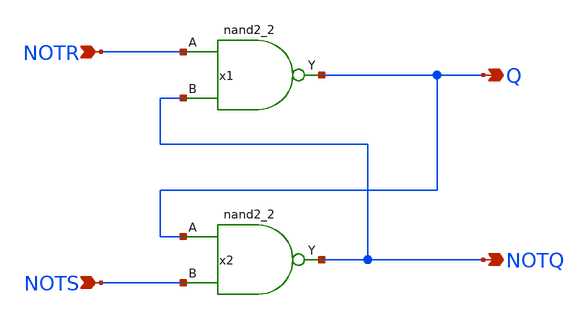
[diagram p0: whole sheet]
** sch_path: designs/libs/core_analog/oscillator/sr_latch.sch
**.subckt sr_latch NOTR NOTS Q NOTQ
*.ipin NOTR
*.ipin NOTS
*.opin Q
*.opin NOTQ
x1 NOTR NOTQ VSSd VDDd VSSd VDDd Q gf180mcu_fd_sc_mcu9t5v0__nand2_2
x2 Q NOTS VSSd VDDd VSSd VDDd NOTQ gf180mcu_fd_sc_mcu9t5v0__nand2_2
**.ends
.end
